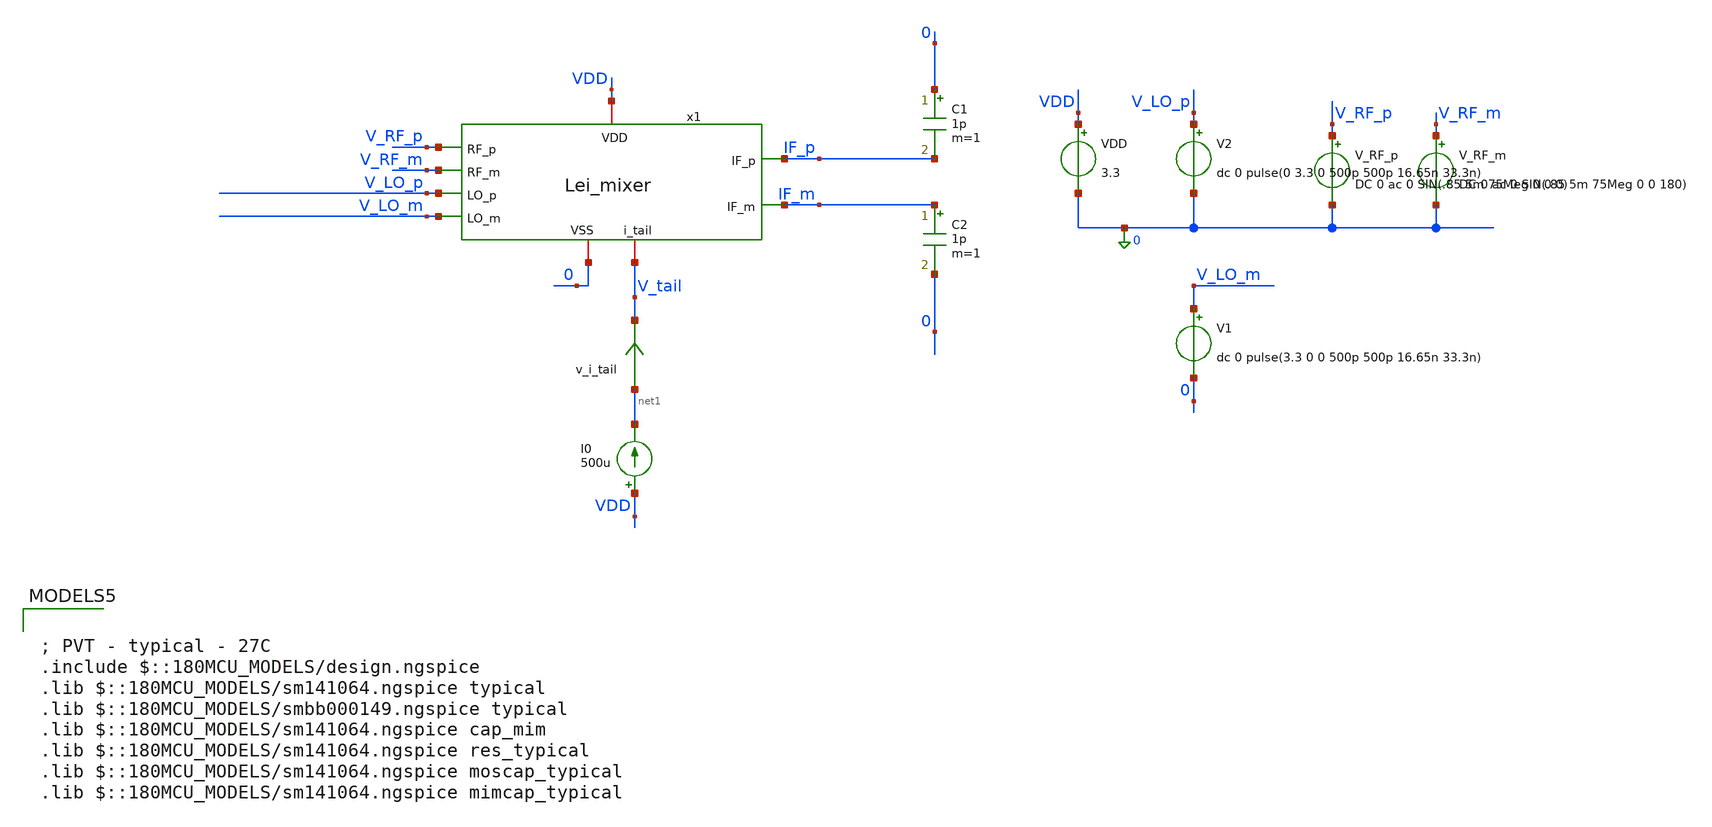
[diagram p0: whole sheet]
** sch_path: designs/mixer/testbench/tb_LEI_pmos_mixer.sch
**.subckt tb_LEI_pmos_mixer
x1 IF_p V_RF_p VDD 0 IF_m V_RF_m V_LO_p V_tail V_LO_m Lei_mixer
VDD VDD 0 3.3
V2 V_LO_p 0 dc 0 pulse(0 3.3 0 500p 500p 16.65n 33.3n)
I0 VDD net1 500u
V_RF_p V_RF_p 0 DC 0 ac 0 SIN(.85 5m 75Meg 0 0 0)
V_RF_m V_RF_m 0 DC 0 ac 0 SIN(.85 5m 75Meg 0 0 180)
v_i_tail net1 V_tail 0
.save i(v_i_tail)
V1 V_LO_m 0 dc 0 pulse(3.3 0 0 500p 500p 16.65n 33.3n)
C1 0 IF_p 1p m=1
C2 IF_m 0 1p m=1
**** begin user architecture code



.control

destroy all
save all
write tb_LEI_pmos_mixer.raw



op
echo RF pair
print @m.x1.xm1.m0[gm]
print @m.x1.xm1.m0[id]
print @m.x1.xm1.m0[vgs]
print @m.x1.xm1.m0[vds]
print @m.x1.xm1.m0[vdsat]

echo LO pair
print @m.x1.xm3.m0[gm]
print @m.x1.xm3.m0[id]
print @m.x1.xm3.m0[vgs]
print @m.x1.xm3.m0[vds]
print @m.x1.xm3.m0[vdsat]

print V(Vtail)
print V(IFp)

save @m.x1.xm1.m0[gm]
save @m.x1.xm3.m0[gm]

dc V_RF_CM 0.01 3.3 0.1

plot V_RF_CM if_p if_m
plot i(v_i_tail) i(v.x1.v_i_branch_1) i(v.x1.v_i_branch_2)
plot @m.x1.xm1.m0[gm] @m.x1.xm3.m0[gm]



tran .1n 10u ;transient sim
let vrf = V(V_RF_p)-V(V_RF_m)
let vif = V(IF_p)-V(IF_m)
let vlo = v_lo_p - v_lo_m
;let vif_filtered = if_p_filtered - if_m_filtered

plot V(V_LO_p) v_LO_m
plot if_p if_m
plot vrf
;plot vif vif_filtered
plot i(v_i_tail) i(v.x1.v_i_branch_1) i(v.x1.v_i_branch_2)

fft vif vrf vlo ;vif_filtered

plot db(vif) vs frequency xlimit 0 200Meg
;plot db(vif_filtered) vs frequency xlimit 0 200MEG
plot db(vrf) vs frequency xlimit 0 200Meg
plot db(vlo) vs frequency xlimit 0 1G
.endc



; PVT - typical - 27C
.include $::180MCU_MODELS/design.ngspice
.lib $::180MCU_MODELS/sm141064.ngspice typical
.lib $::180MCU_MODELS/smbb000149.ngspice typical
.lib $::180MCU_MODELS/sm141064.ngspice cap_mim
.lib $::180MCU_MODELS/sm141064.ngspice res_typical
.lib $::180MCU_MODELS/sm141064.ngspice moscap_typical
.lib $::180MCU_MODELS/sm141064.ngspice mimcap_typical

**** end user architecture code
**.ends

* expanding   symbol:  mixer/schematic/Lei_mixer.sym # of pins=9
** sym_path: designs/mixer/schematic/Lei_mixer.sym
** sch_path: designs/mixer/schematic/Lei_mixer.sch
.subckt Lei_mixer IF_p RF_p VDD VSS IF_m RF_m LO_p i_tail LO_m
*.iopin VDD
*.iopin VSS
*.ipin RF_p
*.ipin RF_m
*.ipin LO_p
*.ipin LO_m
*.opin IF_p
*.opin IF_m
*.iopin i_tail
XM1 net3 RF_p net1 VDD pfet_03v3 L=0.28u W=35u nf=1 ad='int((nf+1)/2) * W/nf * 0.18u' as='int((nf+2)/2) * W/nf * 0.18u'
+ pd='2*int((nf+1)/2) * (W/nf + 0.18u)' ps='2*int((nf+2)/2) * (W/nf + 0.18u)' nrd='0.18u / W' nrs='0.18u / W'
+ sa=0 sb=0 sd=0 m=1
XM2 net4 RF_m net2 VDD pfet_03v3 L=0.28u W=35u nf=1 ad='int((nf+1)/2) * W/nf * 0.18u' as='int((nf+2)/2) * W/nf * 0.18u'
+ pd='2*int((nf+1)/2) * (W/nf + 0.18u)' ps='2*int((nf+2)/2) * (W/nf + 0.18u)' nrd='0.18u / W' nrs='0.18u / W'
+ sa=0 sb=0 sd=0 m=1
XM4 IF_m LO_p net3 VDD pfet_03v3 L=0.28u W=100u nf=10 ad='int((nf+1)/2) * W/nf * 0.18u' as='int((nf+2)/2) * W/nf * 0.18u'
+ pd='2*int((nf+1)/2) * (W/nf + 0.18u)' ps='2*int((nf+2)/2) * (W/nf + 0.18u)' nrd='0.18u / W' nrs='0.18u / W'
+ sa=0 sb=0 sd=0 m=1
XM5 IF_p LO_m net3 VDD pfet_03v3 L=0.28u W=100u nf=10 ad='int((nf+1)/2) * W/nf * 0.18u' as='int((nf+2)/2) * W/nf * 0.18u'
+ pd='2*int((nf+1)/2) * (W/nf + 0.18u)' ps='2*int((nf+2)/2) * (W/nf + 0.18u)' nrd='0.18u / W' nrs='0.18u / W'
+ sa=0 sb=0 sd=0 m=1
XM6 IF_m LO_m net4 VDD pfet_03v3 L=0.28u W=100u nf=10 ad='int((nf+1)/2) * W/nf * 0.18u' as='int((nf+2)/2) * W/nf * 0.18u'
+ pd='2*int((nf+1)/2) * (W/nf + 0.18u)' ps='2*int((nf+2)/2) * (W/nf + 0.18u)' nrd='0.18u / W' nrs='0.18u / W'
+ sa=0 sb=0 sd=0 m=1
XM7 IF_p LO_p net4 VDD pfet_03v3 L=0.28u W=100u nf=10 ad='int((nf+1)/2) * W/nf * 0.18u' as='int((nf+2)/2) * W/nf * 0.18u'
+ pd='2*int((nf+1)/2) * (W/nf + 0.18u)' ps='2*int((nf+2)/2) * (W/nf + 0.18u)' nrd='0.18u / W' nrs='0.18u / W'
+ sa=0 sb=0 sd=0 m=1
R1 IF_m VSS 5k m=1
R2 IF_p VSS 5k m=1
v_i_branch_1 i_tail net1 0
.save i(v_i_branch_1)
v_i_branch_2 i_tail net2 0
.save i(v_i_branch_2)
.ends

.end
